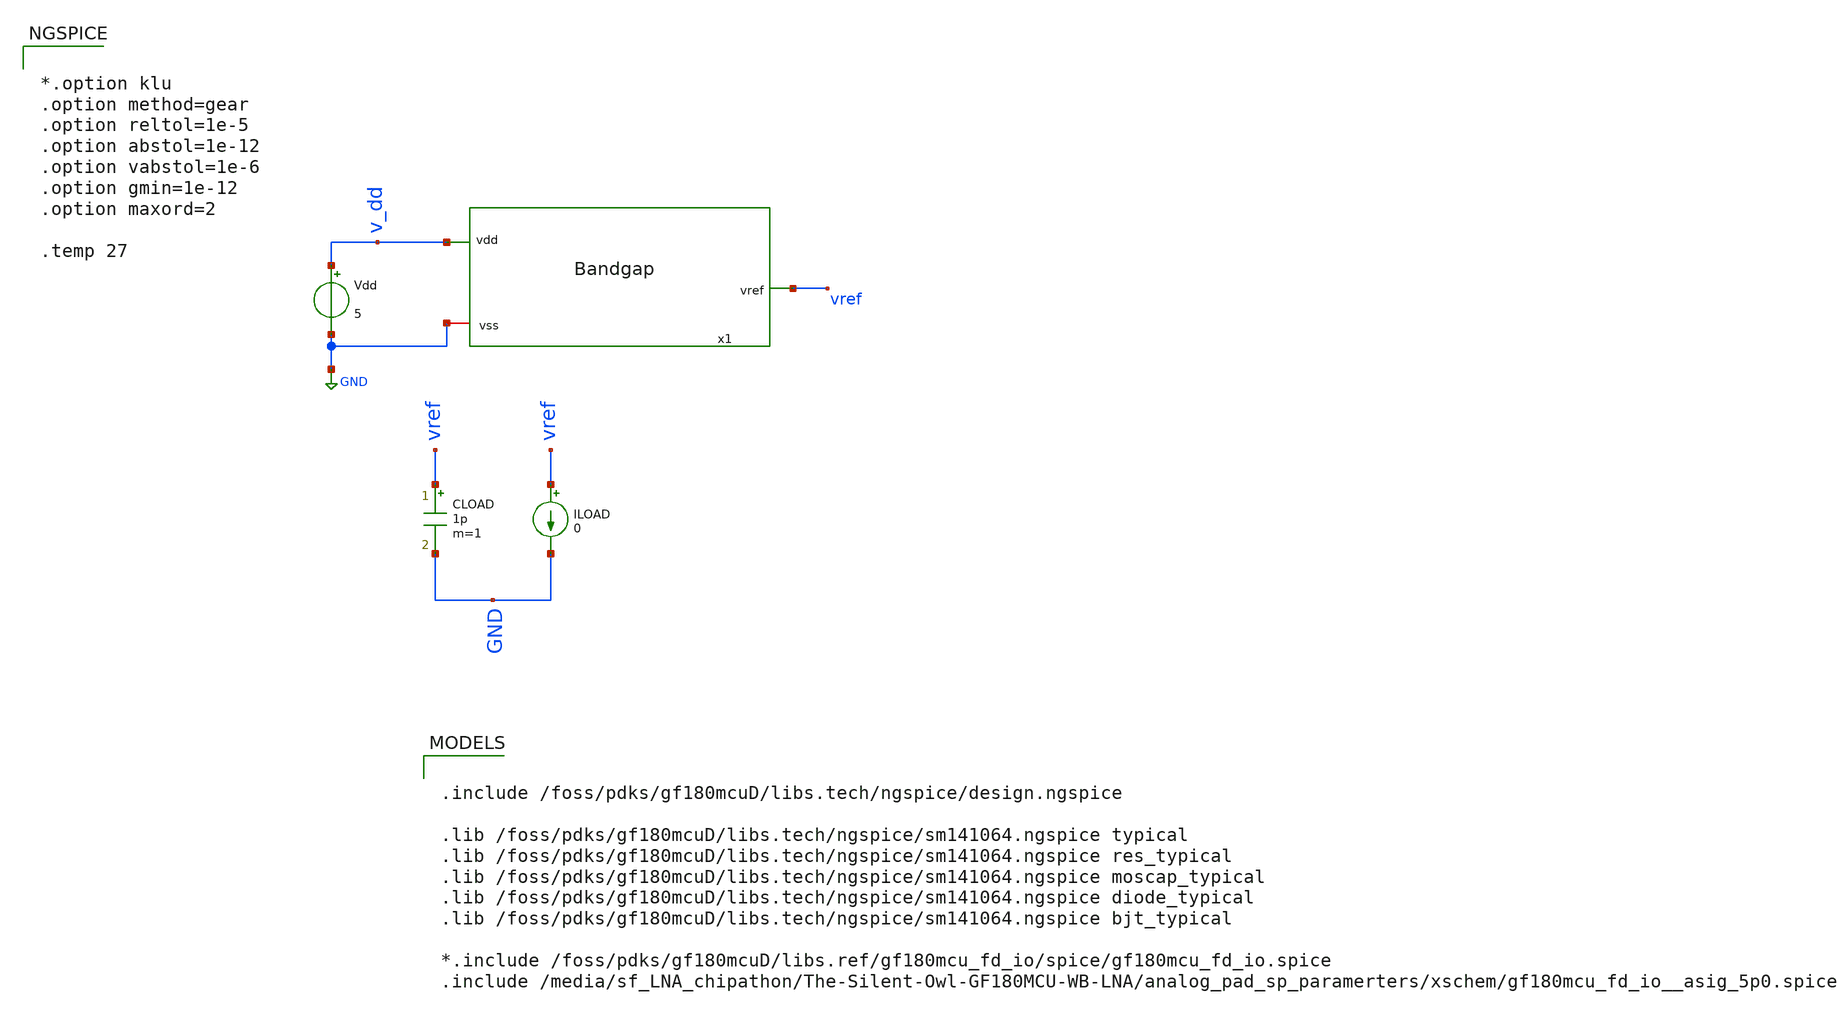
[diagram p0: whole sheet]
** sch_path: xschem/bandgap_tb.sch
**.subckt bandgap_tb
Vdd v_dd GND 5
x1 v_dd vref GND bandgap
CLOAD vref GND 1p m=1
ILOAD vref GND 0
**** begin user architecture code


*.option klu
.option method=gear
.option reltol=1e-5
.option abstol=1e-12
.option vabstol=1e-6
.option gmin=1e-12
.option maxord=2

.temp 27








.control

set filetype=ascii
set numdgt=8
set wr_singlescale

* ============================================================
* Constants
* ============================================================

let t_cold = -30
let t_nom = 27
let t_hot = 125
let temp_span = t_hot - t_cold

* ============================================================
* Create report files
* ============================================================

echo GF180MCU_Bandgap_Ideal_First_Detailed_Report > bandgap_detailed_report.txt
echo ============================================================ >> bandgap_detailed_report.txt
echo . >> bandgap_detailed_report.txt

echo GF180MCU_Bandgap_Ideal_First_Summary > bandgap_summary.txt
echo ============================================================ >> bandgap_summary.txt
echo . >> bandgap_summary.txt

* ============================================================
* Save important results
* ============================================================

save all

* ============================================================
* Print nominal design information
* ============================================================

echo NOMINAL_DESIGN_PARAMETERS >> bandgap_detailed_report.txt
echo ------------------------------------------------------------ >> bandgap_detailed_report.txt
echo VDDNOM_V = 5 >> bandgap_detailed_report.txt
echo QBIG = 40 >> bandgap_detailed_report.txt
echo QSMALL = 2 >> bandgap_detailed_report.txt
echo BJT_RATIO_QBIG_OVER_QSMALL = 20 >> bandgap_detailed_report.txt
echo RPTAT_OHM = 6000 >> bandgap_detailed_report.txt
echo RREF_OHM = 39000 >> bandgap_detailed_report.txt
echo RBIAS_OHM = 10000 >> bandgap_detailed_report.txt
echo PMOS_MAIN_W_L_NF = 50u_1u_1 >> bandgap_detailed_report.txt
echo NMOS_MAIN_W_L_NF = 15u_1u_1 >> bandgap_detailed_report.txt
echo STARTUP_PMOS_W_L_NF = 0.5u_10u_1 >> bandgap_detailed_report.txt
echo . >> bandgap_detailed_report.txt

* ============================================================
* 1. Nominal operating point
* ============================================================

alter Vdd = 5
alter Iload = 0

op

let idd_op = -i(vdd)
let pdc_op = v(v_dd) * idd_op

echo 1_NOMINAL_OPERATING_POINT_T_27C_VDD_5V >> bandgap_detailed_report.txt
echo ------------------------------------------------------------ >> bandgap_detailed_report.txt
print v(vref) >> bandgap_detailed_report.txt
print v(v_dd) >> bandgap_detailed_report.txt
print idd_op >> bandgap_detailed_report.txt
print pdc_op >> bandgap_detailed_report.txt
echo . >> bandgap_detailed_report.txt

echo INTERNAL_BIAS_NODES >> bandgap_detailed_report.txt
print v(x1.vg1) >> bandgap_detailed_report.txt
print v(x1.vg2) >> bandgap_detailed_report.txt
print v(x1.vg3) >> bandgap_detailed_report.txt
print v(x1.vg4) >> bandgap_detailed_report.txt
print v(x1.net1) >> bandgap_detailed_report.txt
print v(x1.net2) >> bandgap_detailed_report.txt
print v(x1.net3) >> bandgap_detailed_report.txt
print v(x1.net4) >> bandgap_detailed_report.txt
print v(x1.net5) >> bandgap_detailed_report.txt
print v(x1.net6) >> bandgap_detailed_report.txt
print v(x1.net7) >> bandgap_detailed_report.txt
print v(x1.net8) >> bandgap_detailed_report.txt
print v(x1.net9) >> bandgap_detailed_report.txt
echo . >> bandgap_detailed_report.txt

write bandgap_op.raw

* ============================================================
* 2. Temperature sweep
* ============================================================

dc temp -30 125 1

meas dc vref_cold find v(vref) at=-30
meas dc vref_nom find v(vref) at=27
meas dc vref_hot find v(vref) at=125
meas dc vref_min min v(vref) from=-30 to=125
meas dc vref_max max v(vref) from=-30 to=125

let vref_span = vref_max - vref_min
let vref_end_delta = vref_hot - vref_cold
let tempco_endpoint_ppm = 1e6 * vref_end_delta / (vref_nom * temp_span)
let tempco_span_ppm = 1e6 * vref_span / (vref_nom * temp_span)
let idd_temp = -i(vdd)

echo 2_TEMPERATURE_SWEEP_MINUS30C_TO_125C >> bandgap_detailed_report.txt
echo ------------------------------------------------------------ >> bandgap_detailed_report.txt
echo VREF_COLD_V = $&vref_cold >> bandgap_detailed_report.txt
echo VREF_NOMINAL_V = $&vref_nom >> bandgap_detailed_report.txt
echo VREF_HOT_V = $&vref_hot >> bandgap_detailed_report.txt
echo VREF_MIN_V = $&vref_min >> bandgap_detailed_report.txt
echo VREF_MAX_V = $&vref_max >> bandgap_detailed_report.txt
echo VREF_SPAN_V = $&vref_span >> bandgap_detailed_report.txt
echo ENDPOINT_TEMP_DELTA_V = $&vref_end_delta >> bandgap_detailed_report.txt
echo ENDPOINT_TEMP_COEFF_PPM_PER_C = $&tempco_endpoint_ppm >> bandgap_detailed_report.txt
echo WORST_SPAN_TEMP_COEFF_PPM_PER_C = $&tempco_span_ppm >> bandgap_detailed_report.txt
echo . >> bandgap_detailed_report.txt

wrdata bandgap_temp_sweep.txt v(vref) idd_temp
write bandgap_temp.raw

* ============================================================
* 3. Supply sweep and line regulation
* ============================================================

alter Iload = 0
dc Vdd 3.0 5.5 0.01

meas dc vref_vdd3p0 find v(vref) at=3.0
meas dc vref_vdd5p0 find v(vref) at=5.0
meas dc vref_line_min min v(vref) from=3.0 to=5.5
meas dc vref_line_max max v(vref) from=3.0 to=5.5

let vref_line_span = vref_line_max - vref_line_min
let line_reg_mv_per_v = 1000 * (vref_line_max - vref_line_min) / (5.5 - 3.0)
let idd_line = -i(vdd)

echo 3_SUPPLY_SWEEP_LINE_REGULATION_3V_TO_5P5V >> bandgap_detailed_report.txt
echo ------------------------------------------------------------ >> bandgap_detailed_report.txt
echo VREF_AT_VDD_3P0_V = $&vref_vdd3p0 >> bandgap_detailed_report.txt
echo VREF_AT_VDD_5P0_V = $&vref_vdd5p0 >> bandgap_detailed_report.txt
echo VREF_LINE_MAX_V = $&vref_line_max >> bandgap_detailed_report.txt
echo VREF_LINE_MIN_V = $&vref_line_min >> bandgap_detailed_report.txt
echo VREF_LINE_SPAN_V = $&vref_line_span >> bandgap_detailed_report.txt
echo LINE_REG_MV_PER_V = $&line_reg_mv_per_v >> bandgap_detailed_report.txt
echo . >> bandgap_detailed_report.txt

wrdata bandgap_line_sweep.txt v(vref) idd_line
write bandgap_line.raw

echo LINE_RESULTS >> bandgap_summary.txt
echo VREF_AT_VDD_3P0_V = $&vref_vdd3p0 >> bandgap_summary.txt
echo VREF_AT_VDD_5P0_V = $&vref_vdd5p0 >> bandgap_summary.txt
echo LINE_REG_MV_PER_V = $&line_reg_mv_per_v >> bandgap_summary.txt
echo . >> bandgap_summary.txt

* ============================================================
* 4. Load regulation
* Requires Iload vref GND 0 in testbench
* ============================================================

alter Vdd = 5
alter Iload = 0

dc Iload 0 1u 0.01u

meas dc vref_load0 find v(vref) at=0
meas dc vref_load100n find v(vref) at=100n
meas dc vref_load500n find v(vref) at=500n
meas dc vref_load1u find v(vref) at=1u
meas dc vref_load_min min v(vref) from=0 to=1u
meas dc vref_load_max max v(vref) from=0 to=1u

let load_reg_0_1u_mv = 1000 * (vref_load1u - vref_load0)
let load_reg_uv_per_ua = 1e6 * (vref_load1u - vref_load0)
let idd_load = -i(vdd)
echo 4_LOAD_REGULATION_0_TO_1UA >> bandgap_detailed_report.txt
echo ------------------------------------------------------------ >> bandgap_detailed_report.txt
echo VREF_AT_ILOAD_0UA_V = $&vref_load0 >> bandgap_detailed_report.txt
echo VREF_AT_ILOAD_100NA_V = $&vref_load100n >> bandgap_detailed_report.txt
echo VREF_AT_ILOAD_500NA_V = $&vref_load500n >> bandgap_detailed_report.txt
echo VREF_AT_ILOAD_1UA_V = $&vref_load1u >> bandgap_detailed_report.txt
echo VREF_LOAD_MIN_V = $&vref_load_min >> bandgap_detailed_report.txt
echo VREF_LOAD_MAX_V = $&vref_load_max >> bandgap_detailed_report.txt
echo LOAD_REG_0_TO_1UA_MV = $&load_reg_0_1u_mv >> bandgap_detailed_report.txt
echo LOAD_REG_UV_PER_UA = $&load_reg_uv_per_ua >> bandgap_detailed_report.txt
echo . >> bandgap_detailed_report.txt

wrdata bandgap_load_sweep.txt v(vref) idd_load
write bandgap_load.raw

echo LOAD_RESULTS >> bandgap_summary.txt
echo VREF_AT_ILOAD_0UA_V = $&vref_load0 >> bandgap_summary.txt
echo VREF_AT_ILOAD_1UA_V = $&vref_load1u >> bandgap_summary.txt
echo LOAD_REG_0_TO_1UA_MV = $&load_reg_0_1u_mv >> bandgap_summary.txt
echo LOAD_REG_UV_PER_UA = $&load_reg_uv_per_ua >> bandgap_summary.txt
echo . >> bandgap_summary.txt
* ============================================================
* 5. Startup transient
* Uses VDD step from 0V to 5V by alter before transient
* ============================================================

alter Vdd = 0
alter Iload = 0
op

alter Vdd = 5

tran 1u 10m uic

meas tran vref_start_100us find v(vref) at=100u
meas tran vref_start_1ms find v(vref) at=1m
meas tran vref_start_5ms find v(vref) at=5m
meas tran vref_start_10ms find v(vref) at=10m

let idd_start = -i(vdd)

echo 5_STARTUP_TRANSIENT_FROM_ZERO_SUPPLY >> bandgap_detailed_report.txt
echo ------------------------------------------------------------ >> bandgap_detailed_report.txt
echo VREF_AT_100US_V = $&vref_start_100us >> bandgap_detailed_report.txt
echo VREF_AT_1MS_V = $&vref_start_1ms >> bandgap_detailed_report.txt
echo VREF_AT_5MS_V = $&vref_start_5ms >> bandgap_detailed_report.txt
echo VREF_AT_10MS_V = $&vref_start_10ms >> bandgap_detailed_report.txt
echo . >> bandgap_detailed_report.txt

wrdata bandgap_startup.txt v(vref) v(x1.vg1) v(x1.vg2) v(x1.vg3) v(x1.vg4) idd_start
write bandgap_startup.raw
echo STARTUP_RESULTS >> bandgap_summary.txt
echo STARTUP_VREF_100US_V = $&vref_start_100us >> bandgap_summary.txt
echo STARTUP_VREF_1MS_V = $&vref_start_1ms >> bandgap_summary.txt
echo STARTUP_VREF_10MS_V = $&vref_start_10ms >> bandgap_summary.txt
echo . >> bandgap_summary.txt

echo TEMP_RESULTS >> bandgap_summary.txt
echo VREF_NOMINAL_27C_V = $&vref_nom >> bandgap_summary.txt
echo VREF_COLD_MINUS30C_V = $&vref_cold >> bandgap_summary.txt
echo VREF_HOT_125C_V = $&vref_hot >> bandgap_summary.txt
echo ENDPOINT_TEMP_COEFF_PPM_PER_C = $&tempco_endpoint_ppm >> bandgap_summary.txt
echo WORST_SPAN_TEMP_COEFF_PPM_PER_C = $&tempco_span_ppm >> bandgap_summary.txt
echo . >> bandgap_summary.txt


.endc



.include /foss/pdks/gf180mcuD/libs.tech/ngspice/design.ngspice

.lib /foss/pdks/gf180mcuD/libs.tech/ngspice/sm141064.ngspice typical
.lib /foss/pdks/gf180mcuD/libs.tech/ngspice/sm141064.ngspice res_typical
.lib /foss/pdks/gf180mcuD/libs.tech/ngspice/sm141064.ngspice moscap_typical
.lib /foss/pdks/gf180mcuD/libs.tech/ngspice/sm141064.ngspice diode_typical
.lib /foss/pdks/gf180mcuD/libs.tech/ngspice/sm141064.ngspice bjt_typical

*.include /foss/pdks/gf180mcuD/libs.ref/gf180mcu_fd_io/spice/gf180mcu_fd_io.spice
.include /media/sf_LNA_chipathon/The-Silent-Owl-GF180MCU-WB-LNA/analog_pad_sp_paramerters/xschem/gf180mcu_fd_io__asig_5p0.spice

**** end user architecture code
**.ends

* expanding   symbol:  bandgap.sym # of pins=3
** sym_path: xschem/bandgap.sym
** sch_path: xschem/bandgap.sch
.subckt bandgap vdd vref vss
*.ipin vdd
*.iopin vss
*.opin vref
XQ1 vss vss net4 pnp_05p00x05p00 m=40 par=40
XQ2 vss vss net6 pnp_05p00x05p00 m=40 par=40
XQ3 vss vss net9 pnp_05p00x05p00 m=2 par=2
XM12 net2 vg4 vdd vdd pfet_05v0 L=1u W=50u nf=10 ad='int((nf+1)/2) * W/nf * 0.18u' as='int((nf+2)/2) * W/nf * 0.18u'
+ pd='2*int((nf+1)/2) * (W/nf + 0.18u)' ps='2*int((nf+2)/2) * (W/nf + 0.18u)' nrd='0.18u / W' nrs='0.18u / W'
+ sa=0 sb=0 sd=0 m=1
XM13 vg3 vg2 net5 vss nfet_05v0 L=1u W=15u nf=3 ad='int((nf+1)/2) * W/nf * 0.18u' as='int((nf+2)/2) * W/nf * 0.18u'
+ pd='2*int((nf+1)/2) * (W/nf + 0.18u)' ps='2*int((nf+2)/2) * (W/nf + 0.18u)' nrd='0.18u / W' nrs='0.18u / W'
+ sa=0 sb=0 sd=0 m=1
XM14 net1 vg4 vdd vdd pfet_05v0 L=1u W=50u nf=10 ad='int((nf+1)/2) * W/nf * 0.18u' as='int((nf+2)/2) * W/nf * 0.18u'
+ pd='2*int((nf+1)/2) * (W/nf + 0.18u)' ps='2*int((nf+2)/2) * (W/nf + 0.18u)' nrd='0.18u / W' nrs='0.18u / W'
+ sa=0 sb=0 sd=0 m=1
XM1 vg2 vg3 net1 vdd pfet_05v0 L=1u W=50u nf=10 ad='int((nf+1)/2) * W/nf * 0.18u' as='int((nf+2)/2) * W/nf * 0.18u'
+ pd='2*int((nf+1)/2) * (W/nf + 0.18u)' ps='2*int((nf+2)/2) * (W/nf + 0.18u)' nrd='0.18u / W' nrs='0.18u / W'
+ sa=0 sb=0 sd=0 m=1
XM2 vg4 vg3 net2 vdd pfet_05v0 L=1u W=50u nf=10 ad='int((nf+1)/2) * W/nf * 0.18u' as='int((nf+2)/2) * W/nf * 0.18u'
+ pd='2*int((nf+1)/2) * (W/nf + 0.18u)' ps='2*int((nf+2)/2) * (W/nf + 0.18u)' nrd='0.18u / W' nrs='0.18u / W'
+ sa=0 sb=0 sd=0 m=1
XM3 net3 vg4 vdd vdd pfet_05v0 L=1u W=50u nf=10 ad='int((nf+1)/2) * W/nf * 0.18u' as='int((nf+2)/2) * W/nf * 0.18u'
+ pd='2*int((nf+1)/2) * (W/nf + 0.18u)' ps='2*int((nf+2)/2) * (W/nf + 0.18u)' nrd='0.18u / W' nrs='0.18u / W'
+ sa=0 sb=0 sd=0 m=1
XM4 vref vg3 net3 vdd pfet_05v0 L=1u W=50u nf=10 ad='int((nf+1)/2) * W/nf * 0.18u' as='int((nf+2)/2) * W/nf * 0.18u'
+ pd='2*int((nf+1)/2) * (W/nf + 0.18u)' ps='2*int((nf+2)/2) * (W/nf + 0.18u)' nrd='0.18u / W' nrs='0.18u / W'
+ sa=0 sb=0 sd=0 m=1
XM5 vg2 vg2 vg3 vdd pfet_05v0 L=10u W=0.5u nf=1 ad='int((nf+1)/2) * W/nf * 0.18u' as='int((nf+2)/2) * W/nf * 0.18u'
+ pd='2*int((nf+1)/2) * (W/nf + 0.18u)' ps='2*int((nf+2)/2) * (W/nf + 0.18u)' nrd='0.18u / W' nrs='0.18u / W'
+ sa=0 sb=0 sd=0 m=1
XM6 vg1 vg2 net8 vss nfet_05v0 L=1u W=15u nf=3 ad='int((nf+1)/2) * W/nf * 0.18u' as='int((nf+2)/2) * W/nf * 0.18u'
+ pd='2*int((nf+1)/2) * (W/nf + 0.18u)' ps='2*int((nf+2)/2) * (W/nf + 0.18u)' nrd='0.18u / W' nrs='0.18u / W'
+ sa=0 sb=0 sd=0 m=1
XM9 net8 vg1 net9 vss nfet_05v0 L=1u W=15u nf=3 ad='int((nf+1)/2) * W/nf * 0.18u' as='int((nf+2)/2) * W/nf * 0.18u'
+ pd='2*int((nf+1)/2) * (W/nf + 0.18u)' ps='2*int((nf+2)/2) * (W/nf + 0.18u)' nrd='0.18u / W' nrs='0.18u / W'
+ sa=0 sb=0 sd=0 m=1
XM7 net5 vg1 net7 vss nfet_05v0 L=1u W=15u nf=3 ad='int((nf+1)/2) * W/nf * 0.18u' as='int((nf+2)/2) * W/nf * 0.18u'
+ pd='2*int((nf+1)/2) * (W/nf + 0.18u)' ps='2*int((nf+2)/2) * (W/nf + 0.18u)' nrd='0.18u / W' nrs='0.18u / W'
+ sa=0 sb=0 sd=0 m=1
XR6 net6 net7 vss ppolyf_u_1k_6p0 r_width=3u r_length=18u m=1
XR7 net4 vref vss ppolyf_u_1k_6p0 r_width=3u r_length=116.2u m=1
XR8 vg1 vg2 vss ppolyf_u_1k_6p0 r_width=3u r_length=30u m=1
XR5 vg3 vg4 vss ppolyf_u_1k_6p0 r_width=3u r_length=30u m=1
.ends

.GLOBAL GND
.end
